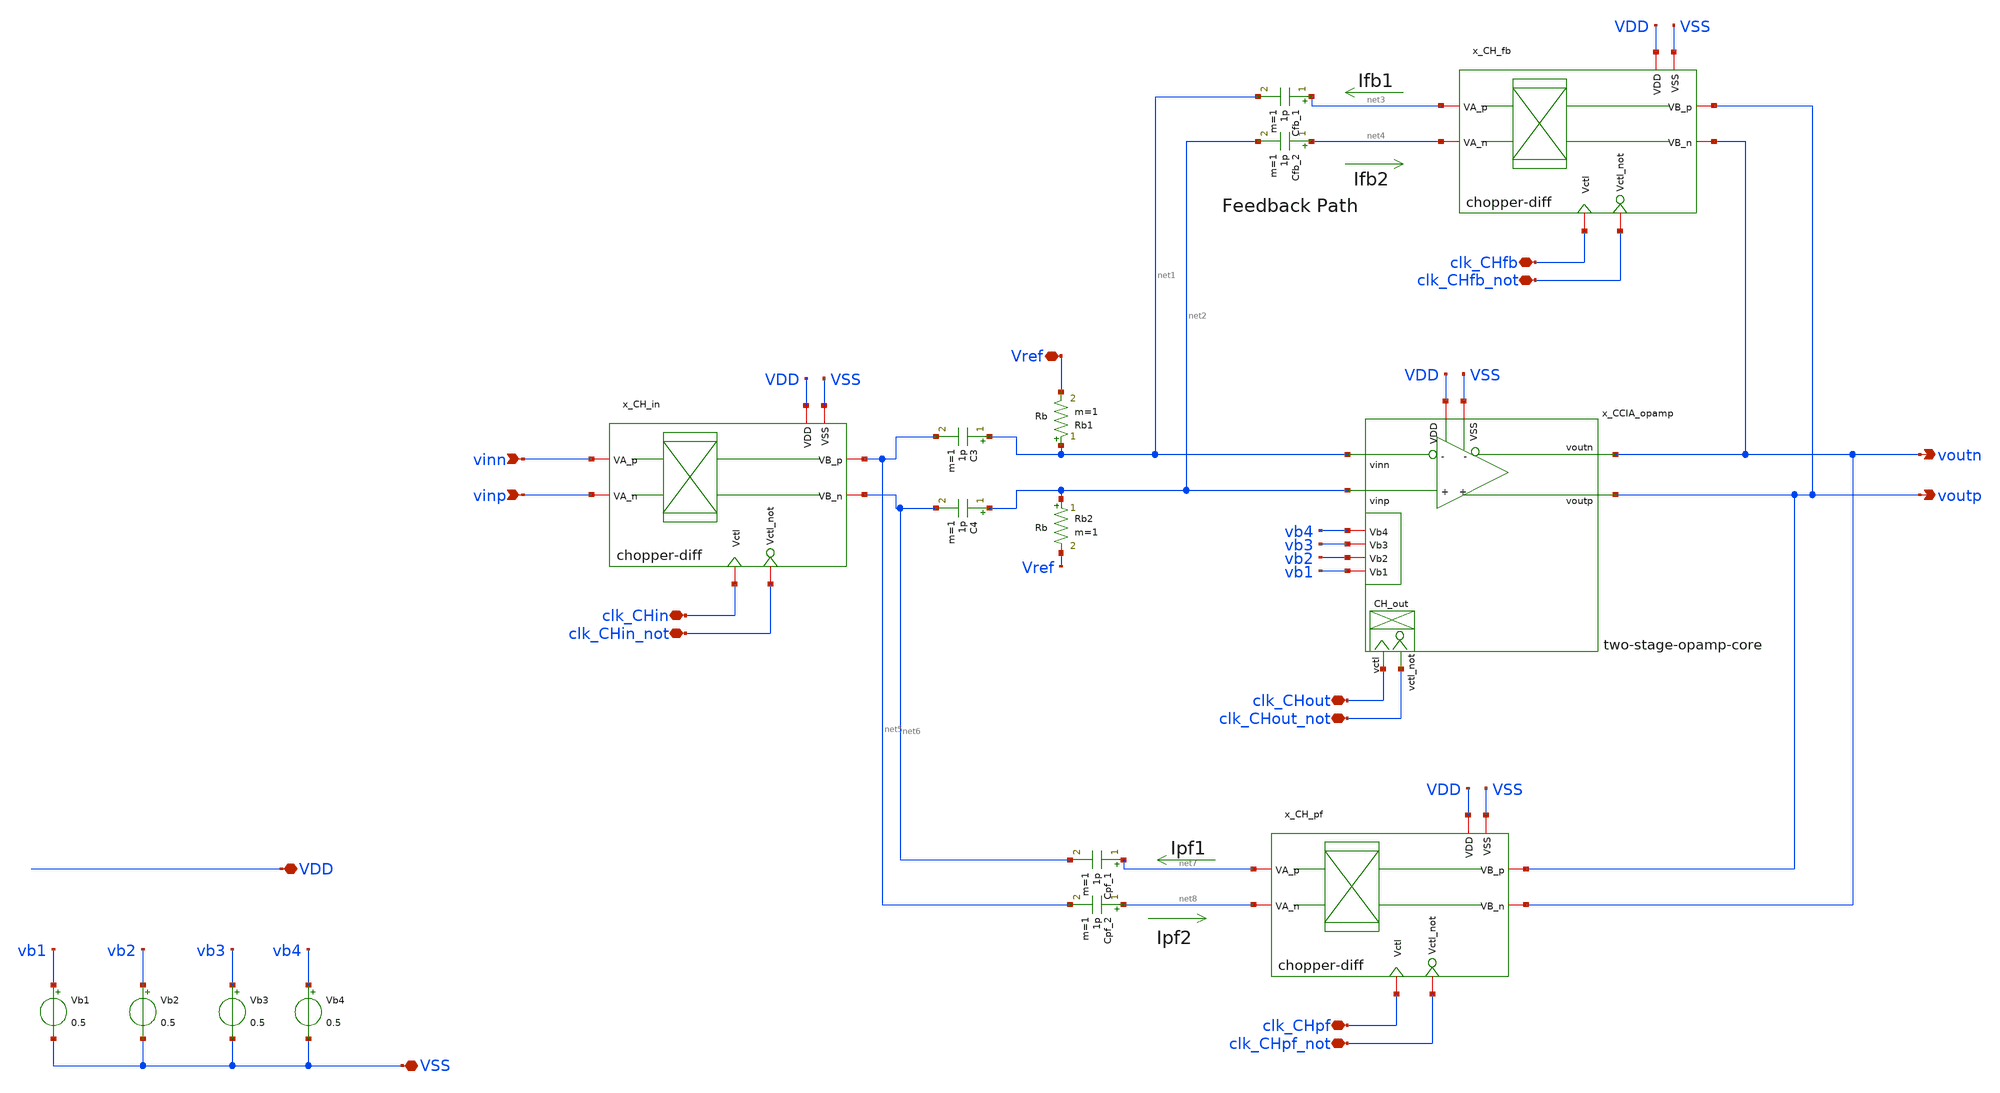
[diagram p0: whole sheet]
** sch_path: analog-db/drawings/ccia-02-QinwenFan-chopper-ripple-reduction/ccia-dut-chopper-w-positive-feedback.sch
* Copyright 2026 MacAnalog Research Group
**.subckt ccia-dut-chopper-w-positive-feedback VSS VDD voutn voutp clk_CHout clk_CHout_not clk_CHfb
*+ clk_CHfb_not clk_CHin clk_CHin_not vinn vinp Vref clk_CHpf clk_CHpf_not
*.iopin VSS
*.iopin VDD
*.opin voutn
*.opin voutp
*.iopin clk_CHout
*.iopin clk_CHout_not
*.iopin clk_CHfb
*.iopin clk_CHfb_not
*.iopin clk_CHin
*.iopin clk_CHin_not
*.ipin vinn
*.ipin vinp
*.iopin Vref
*.iopin clk_CHpf
*.iopin clk_CHpf_not
x_CCIA_opamp VDD vb4 net1 voutn vb3 net2 vb2 voutp clk_CHout clk_CHout_not vb1 VSS
+ two-stage-opamp-core
Vb1 vb1 VSS 0.5
Vb2 vb2 VSS 0.5
Vb3 vb3 VSS 0.5
x_CH_fb clk_CHfb VDD voutp net3 clk_CHfb_not VSS voutn net4 chopper-diff
Cfb_1 net3 net1 1p m=1
Cfb_2 net4 net2 1p m=1
C3 net1 net5 1p m=1
C4 net2 net6 1p m=1
x_CH_in clk_CHin VDD net5 vinn clk_CHin_not VSS net6 vinp chopper-diff
Rb1 net1 Vref Rb m=1
Rb2 net2 Vref Rb m=1
Vb4 vb4 VSS 0.5
x_CH_pf clk_CHpf VDD voutp net7 clk_CHpf_not VSS voutn net8 chopper-diff
Cpf_1 net7 net6 1p m=1
Cpf_2 net8 net5 1p m=1
**.ends
.end
